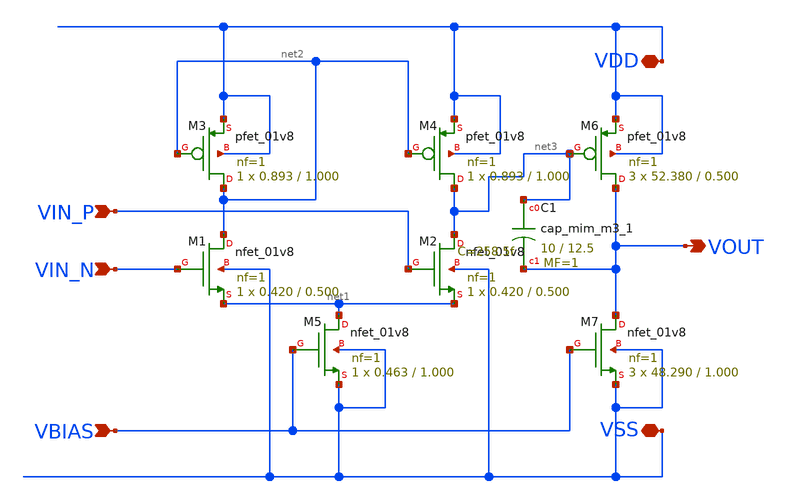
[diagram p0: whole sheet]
** sch_path: analog/bootcamp_opamp/build/schematic/myopamp.sch
**.subckt myopamp VIN_N VIN_P VBIAS VOUT VDD VSS
*.ipin VIN_N
*.ipin VIN_P
*.ipin VBIAS
*.opin VOUT
*.iopin VDD
*.iopin VSS
XM1 net2 VIN_N net1 VSS sky130_fd_pr__nfet_01v8 L=0.500 W=0.420 nf=1 ad='int((nf+1)/2) * W/nf * 0.29'
+ as='int((nf+2)/2) * W/nf * 0.29' pd='2*int((nf+1)/2) * (W/nf + 0.29)' ps='2*int((nf+2)/2) * (W/nf + 0.29)'
+ nrd='0.29 / W' nrs='0.29 / W' sa=0 sb=0 sd=0 mult=1 m=1
XM2 net3 VIN_P net1 VSS sky130_fd_pr__nfet_01v8 L=0.500 W=0.420 nf=1 ad='int((nf+1)/2) * W/nf * 0.29'
+ as='int((nf+2)/2) * W/nf * 0.29' pd='2*int((nf+1)/2) * (W/nf + 0.29)' ps='2*int((nf+2)/2) * (W/nf + 0.29)'
+ nrd='0.29 / W' nrs='0.29 / W' sa=0 sb=0 sd=0 mult=1 m=1
XM3 net2 net2 VDD VDD sky130_fd_pr__pfet_01v8 L=1.000 W=0.893 nf=1 ad='int((nf+1)/2) * W/nf * 0.29' as='int((nf+2)/2) * W/nf * 0.29'
+ pd='2*int((nf+1)/2) * (W/nf + 0.29)' ps='2*int((nf+2)/2) * (W/nf + 0.29)' nrd='0.29 / W' nrs='0.29 / W'
+ sa=0 sb=0 sd=0 mult=1 m=1
XM4 net3 net2 VDD VDD sky130_fd_pr__pfet_01v8 L=1.000 W=0.893 nf=1 ad='int((nf+1)/2) * W/nf * 0.29' as='int((nf+2)/2) * W/nf * 0.29'
+ pd='2*int((nf+1)/2) * (W/nf + 0.29)' ps='2*int((nf+2)/2) * (W/nf + 0.29)' nrd='0.29 / W' nrs='0.29 / W'
+ sa=0 sb=0 sd=0 mult=1 m=1
XM5 net1 VBIAS VSS VSS sky130_fd_pr__nfet_01v8 L=1.000 W=0.463 nf=1 ad='int((nf+1)/2) * W/nf * 0.29'
+ as='int((nf+2)/2) * W/nf * 0.29' pd='2*int((nf+1)/2) * (W/nf + 0.29)' ps='2*int((nf+2)/2) * (W/nf + 0.29)'
+ nrd='0.29 / W' nrs='0.29 / W' sa=0 sb=0 sd=0 mult=1 m=1
XM6 VOUT net3 VDD VDD sky130_fd_pr__pfet_01v8 L=0.500 W=52.380 nf=1 ad='int((nf+1)/2) * W/nf * 0.29'
+ as='int((nf+2)/2) * W/nf * 0.29' pd='2*int((nf+1)/2) * (W/nf + 0.29)' ps='2*int((nf+2)/2) * (W/nf + 0.29)'
+ nrd='0.29 / W' nrs='0.29 / W' sa=0 sb=0 sd=0 mult=3 m=3
XM7 VOUT VBIAS VSS VSS sky130_fd_pr__nfet_01v8 L=1.000 W=48.290 nf=1 ad='int((nf+1)/2) * W/nf * 0.29'
+ as='int((nf+2)/2) * W/nf * 0.29' pd='2*int((nf+1)/2) * (W/nf + 0.29)' ps='2*int((nf+2)/2) * (W/nf + 0.29)'
+ nrd='0.29 / W' nrs='0.29 / W' sa=0 sb=0 sd=0 mult=3 m=3
XC1 net3 VOUT sky130_fd_pr__cap_mim_m3_1 W=10 L=12.5 MF=1 m=1
**.ends
.end
